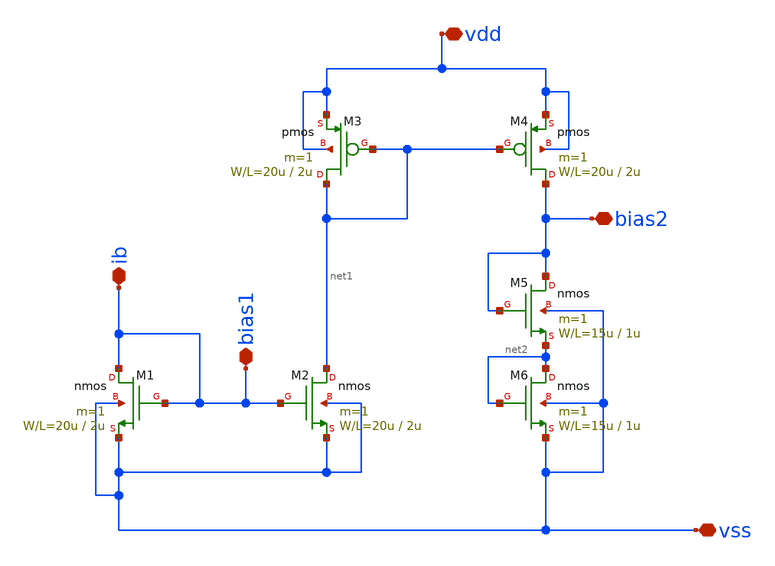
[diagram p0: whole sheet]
** sch_path: member_project/GroupWork/Team_masahiro/bias.sch
**.subckt bias ib vdd vss bias1 bias2
*.iopin ib
*.iopin vdd
*.iopin vss
*.iopin bias1
*.iopin bias2
M1 ib ib vss vss nmos L=2u W=20u m=1
M2 net1 ib vss vss nmos L=2u W=20u m=1
M3 net1 net1 vdd vdd pmos L=2u W=20u m=1
M4 bias2 net1 vdd vdd pmos L=2u W=20u m=1
M5 bias2 bias2 net2 vss nmos L=1u W=15u m=1
M6 net2 net2 vss vss nmos L=1u W=15u m=1
**** begin user architecture code
 .include $::LIB/mos.lib
.include $::LIB/passive.lib
.include $::LIB/diode.lib
**** end user architecture code
**.ends
.end
